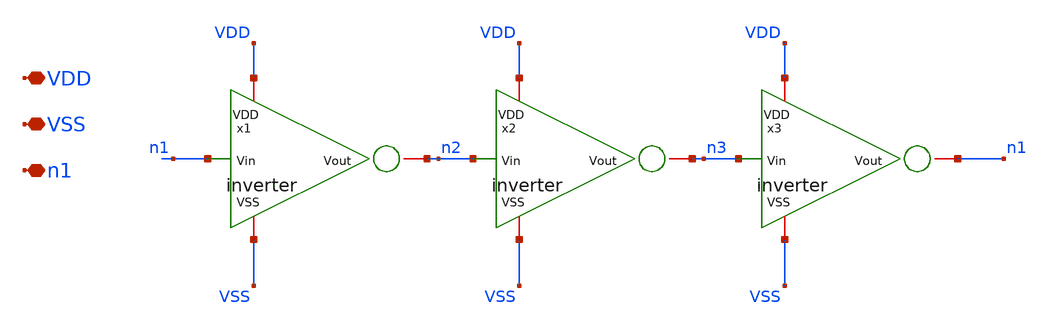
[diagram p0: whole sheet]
** sch_path: Modulo_Analogico/Lab2/3_stage_RO.sch
**.subckt 3_stage_RO VDD VSS n1
*.iopin VDD
*.iopin VSS
*.iopin n1
x1 n1 VDD VSS n2 inverter
x2 n2 VDD VSS n3 inverter
x3 n3 VDD VSS n1 inverter
**.ends
.end
